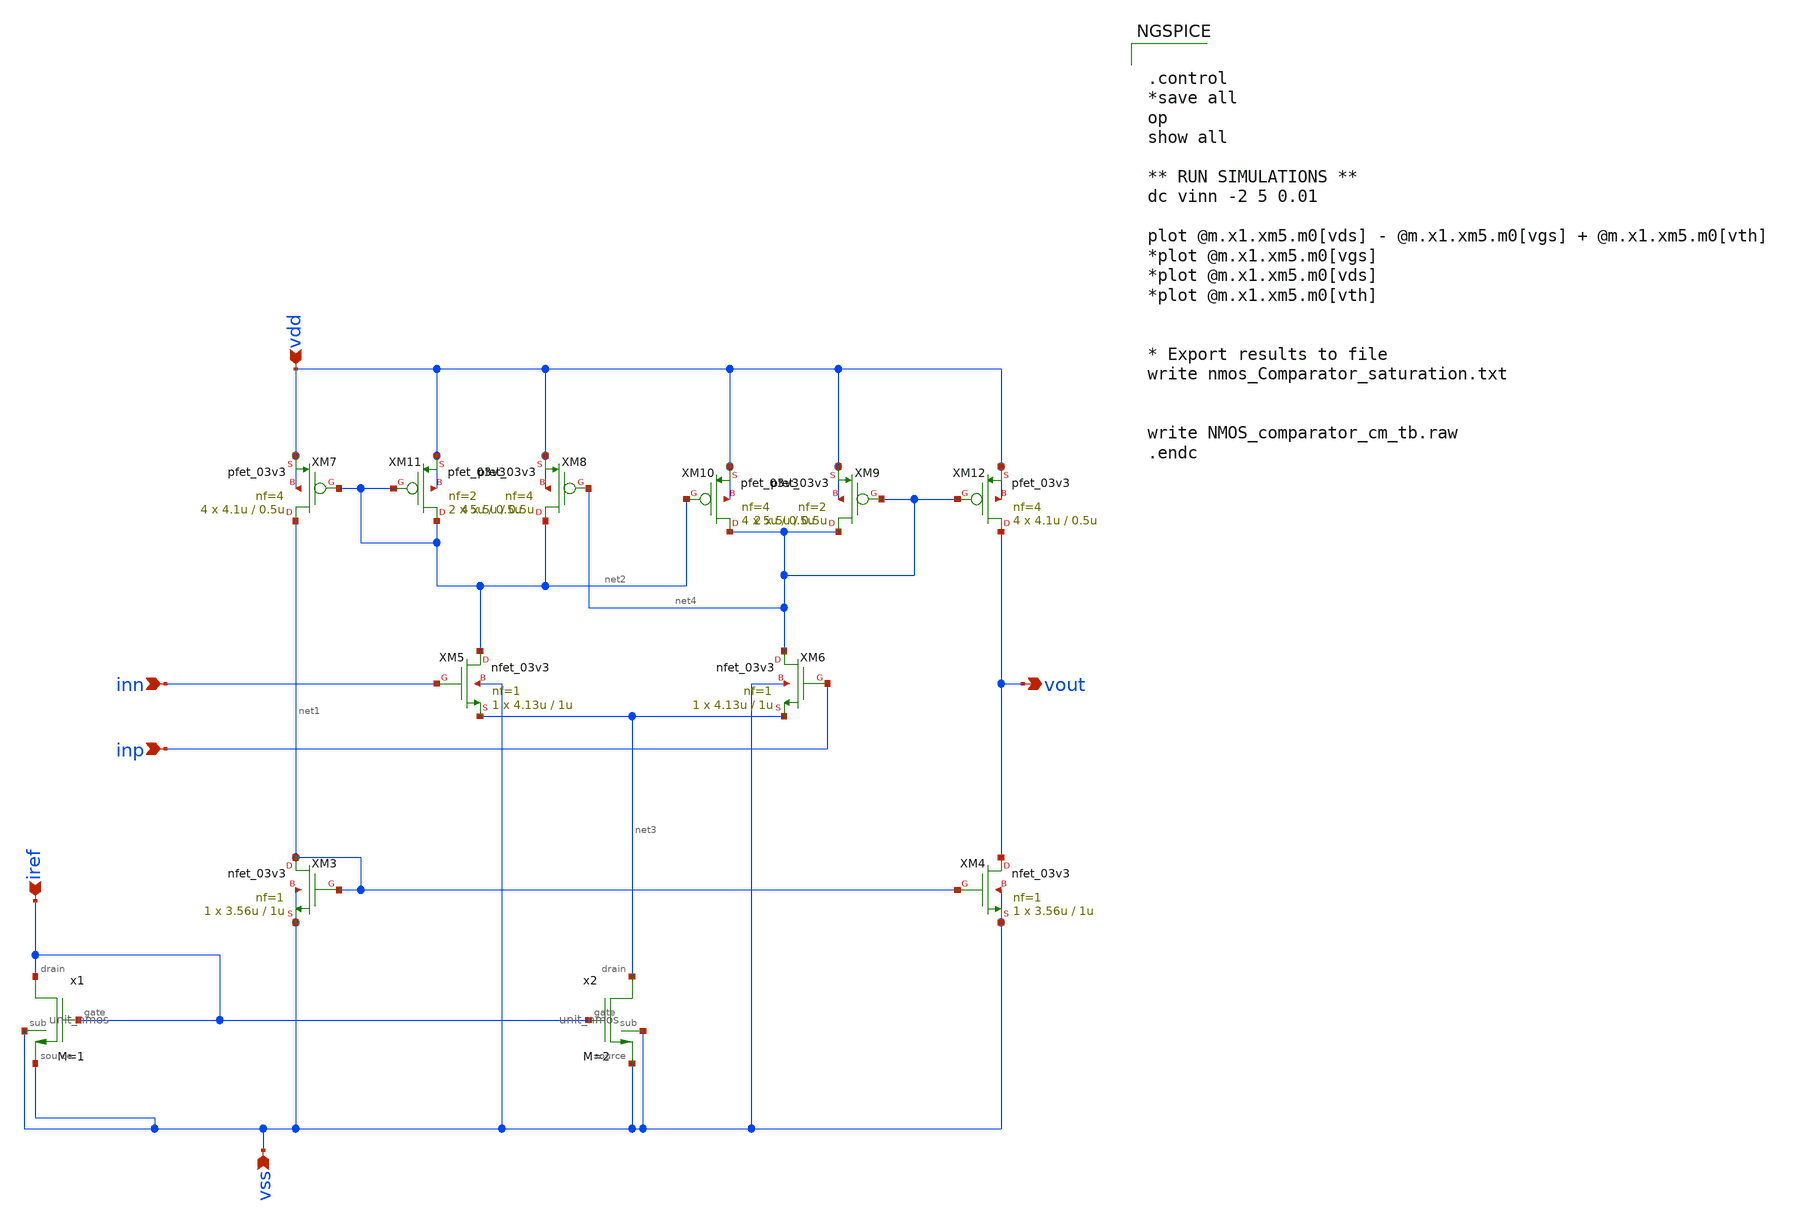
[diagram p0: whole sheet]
** sch_path: designs/switch_matrix_gf180mcu_9t5v0-main/designs/libs/core_analog/Comparator/Nmos_Comparator.sch
**.subckt Nmos_Comparator vss vdd iref inn inp vout
*.ipin vss
*.ipin vdd
*.ipin iref
*.ipin inn
*.ipin inp
*.opin vout
XM3 net1 net1 vss vss nfet_03v3 L=1u W=3.56u nf=1 ad='int((nf+1)/2) * W/nf * 0.18u' as='int((nf+2)/2) * W/nf * 0.18u'
+ pd='2*int((nf+1)/2) * (W/nf + 0.18u)' ps='2*int((nf+2)/2) * (W/nf + 0.18u)' nrd='0.18u / W' nrs='0.18u / W'
+ sa=0 sb=0 sd=0 m=1
XM4 vout net1 vss vss nfet_03v3 L=1u W=3.56u nf=1 ad='int((nf+1)/2) * W/nf * 0.18u' as='int((nf+2)/2) * W/nf * 0.18u'
+ pd='2*int((nf+1)/2) * (W/nf + 0.18u)' ps='2*int((nf+2)/2) * (W/nf + 0.18u)' nrd='0.18u / W' nrs='0.18u / W'
+ sa=0 sb=0 sd=0 m=1
XM5 net2 inn net3 vss nfet_03v3 L=1u W=4.13u nf=1 ad='int((nf+1)/2) * W/nf * 0.18u' as='int((nf+2)/2) * W/nf * 0.18u'
+ pd='2*int((nf+1)/2) * (W/nf + 0.18u)' ps='2*int((nf+2)/2) * (W/nf + 0.18u)' nrd='0.18u / W' nrs='0.18u / W'
+ sa=0 sb=0 sd=0 m=1
XM6 net4 inp net3 vss nfet_03v3 L=1u W=4.13u nf=1 ad='int((nf+1)/2) * W/nf * 0.18u' as='int((nf+2)/2) * W/nf * 0.18u'
+ pd='2*int((nf+1)/2) * (W/nf + 0.18u)' ps='2*int((nf+2)/2) * (W/nf + 0.18u)' nrd='0.18u / W' nrs='0.18u / W'
+ sa=0 sb=0 sd=0 m=1
XM7 net1 net2 vdd vdd pfet_03v3 L=0.5u W=4.1u nf=4 ad='int((nf+1)/2) * W/nf * 0.18u' as='int((nf+2)/2) * W/nf * 0.18u'
+ pd='2*int((nf+1)/2) * (W/nf + 0.18u)' ps='2*int((nf+2)/2) * (W/nf + 0.18u)' nrd='0.18u / W' nrs='0.18u / W'
+ sa=0 sb=0 sd=0 m=4
XM8 net2 net4 vdd vdd pfet_03v3 L=0.5u W=5u nf=4 ad='int((nf+1)/2) * W/nf * 0.18u' as='int((nf+2)/2) * W/nf * 0.18u'
+ pd='2*int((nf+1)/2) * (W/nf + 0.18u)' ps='2*int((nf+2)/2) * (W/nf + 0.18u)' nrd='0.18u / W' nrs='0.18u / W'
+ sa=0 sb=0 sd=0 m=4
XM9 net4 net4 vdd vdd pfet_03v3 L=0.5u W=5u nf=2 ad='int((nf+1)/2) * W/nf * 0.18u' as='int((nf+2)/2) * W/nf * 0.18u'
+ pd='2*int((nf+1)/2) * (W/nf + 0.18u)' ps='2*int((nf+2)/2) * (W/nf + 0.18u)' nrd='0.18u / W' nrs='0.18u / W'
+ sa=0 sb=0 sd=0 m=2
XM10 net4 net2 vdd vdd pfet_03v3 L=0.5u W=5u nf=4 ad='int((nf+1)/2) * W/nf * 0.18u' as='int((nf+2)/2) * W/nf * 0.18u'
+ pd='2*int((nf+1)/2) * (W/nf + 0.18u)' ps='2*int((nf+2)/2) * (W/nf + 0.18u)' nrd='0.18u / W' nrs='0.18u / W'
+ sa=0 sb=0 sd=0 m=4
XM11 net2 net2 vdd vdd pfet_03v3 L=0.5u W=5u nf=2 ad='int((nf+1)/2) * W/nf * 0.18u' as='int((nf+2)/2) * W/nf * 0.18u'
+ pd='2*int((nf+1)/2) * (W/nf + 0.18u)' ps='2*int((nf+2)/2) * (W/nf + 0.18u)' nrd='0.18u / W' nrs='0.18u / W'
+ sa=0 sb=0 sd=0 m=2
XM12 vout net4 vdd vdd pfet_03v3 L=0.5u W=4.1u nf=4 ad='int((nf+1)/2) * W/nf * 0.18u' as='int((nf+2)/2) * W/nf * 0.18u'
+ pd='2*int((nf+1)/2) * (W/nf + 0.18u)' ps='2*int((nf+2)/2) * (W/nf + 0.18u)' nrd='0.18u / W' nrs='0.18u / W'
+ sa=0 sb=0 sd=0 m=4
x1 iref vss iref vss unit_nmos M=1
x2 net3 vss iref vss unit_nmos M=2
**** begin user architecture code


.control
*save all
op
show all

** RUN SIMULATIONS **
dc vinn -2 5 0.01

plot @m.x1.xm5.m0[vds] - @m.x1.xm5.m0[vgs] + @m.x1.xm5.m0[vth]
*plot @m.x1.xm5.m0[vgs]
*plot @m.x1.xm5.m0[vds]
*plot @m.x1.xm5.m0[vth]


* Export results to file
write nmos_Comparator_saturation.txt


write NMOS_comparator_cm_tb.raw
.endc


**** end user architecture code
**.ends
.end
